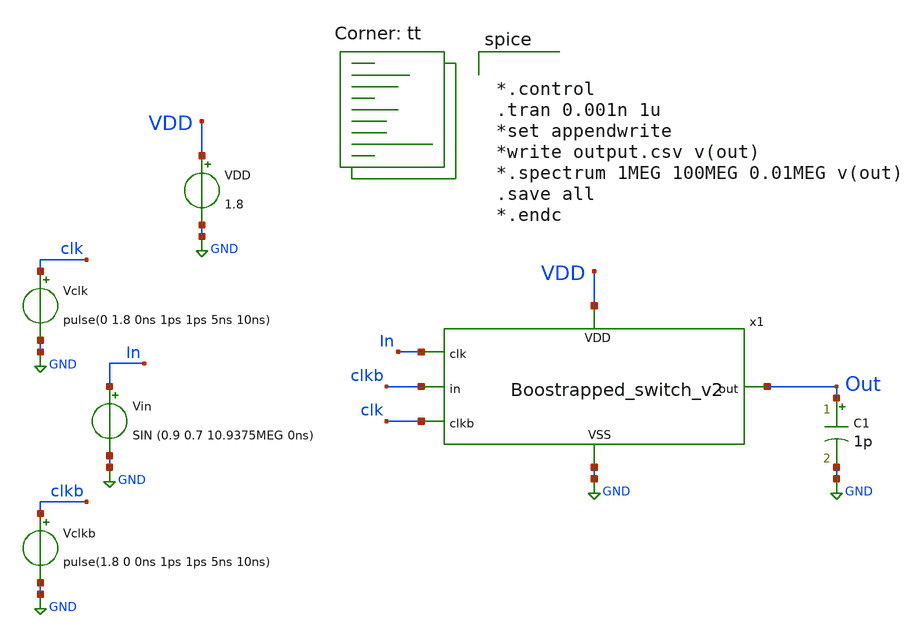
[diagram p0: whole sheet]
** sch_path: SampleHold/Boostrapped_switch_v2_tb.sch
**.subckt Boostrapped_switch_v2_tb
Vclk clk GND pulse(0 1.8 0ns 1ps 1ps 5ns 10ns)
Vin In GND SIN (0.9 0.7 10.9375MEG 0ns)
VDD VDD GND 1.8
Vclkb clkb GND pulse(1.8 0 0ns 1ps 1ps 5ns 10ns)
C1 Out GND 1p m=1
x1 clkb In clk GND Out VDD Boostrapped_switch_v2
**** begin user architecture code
.lib $::SKYWATER_MODELS/sky130.lib.spice tt


*.control
.tran 0.001n 1u
*set appendwrite
*write output.csv v(out)
*.spectrum 1MEG 100MEG 0.01MEG v(out)
.save all
*.endc


**** end user architecture code
**.ends

* expanding   symbol:  project/SampleHold/Boostrapped_switch_v2.sym # of pins=6
** sym_path: SampleHold/Boostrapped_switch_v2.sym
** sch_path: SampleHold/Boostrapped_switch_v2.sch
.subckt Boostrapped_switch_v2 in clk clkb VSS out VDD
*.ipin in
*.opin out
*.ipin VSS
*.ipin VDD
*.ipin clkb
*.ipin clk
XM1 net4 clkb net5 VSS sky130_fd_pr__nfet_01v8 L=0.15 W=2 nf=1 ad='int((nf+1)/2) * W/nf * 0.29' as='int((nf+2)/2) * W/nf * 0.29'
+ pd='2*int((nf+1)/2) * (W/nf + 0.29)' ps='2*int((nf+2)/2) * (W/nf + 0.29)' nrd='0.29 / W' nrs='0.29 / W'
+ sa=0 sb=0 sd=0 mult=1 m=1
XM2 in clk net4 VSS sky130_fd_pr__nfet_01v8 L=0.15 W=6 nf=1 ad='int((nf+1)/2) * W/nf * 0.29' as='int((nf+2)/2) * W/nf * 0.29'
+ pd='2*int((nf+1)/2) * (W/nf + 0.29)' ps='2*int((nf+2)/2) * (W/nf + 0.29)' nrd='0.29 / W' nrs='0.29 / W'
+ sa=0 sb=0 sd=0 mult=1 m=1
XM3 net1 Vg net2 net2 sky130_fd_pr__pfet_01v8 L=0.15 W=2 nf=1 ad='int((nf+1)/2) * W/nf * 0.29' as='int((nf+2)/2) * W/nf * 0.29'
+ pd='2*int((nf+1)/2) * (W/nf + 0.29)' ps='2*int((nf+2)/2) * (W/nf + 0.29)' nrd='0.29 / W' nrs='0.29 / W'
+ sa=0 sb=0 sd=0 mult=1 m=1
XM4 Vg clkb net2 net2 sky130_fd_pr__pfet_01v8 L=0.15 W=6 nf=1 ad='int((nf+1)/2) * W/nf * 0.29' as='int((nf+2)/2) * W/nf * 0.29'
+ pd='2*int((nf+1)/2) * (W/nf + 0.29)' ps='2*int((nf+2)/2) * (W/nf + 0.29)' nrd='0.29 / W' nrs='0.29 / W'
+ sa=0 sb=0 sd=0 mult=1 m=1
XM5 out Vg in VSS sky130_fd_pr__nfet_01v8 L=0.15 W=12 nf=1 ad='int((nf+1)/2) * W/nf * 0.29' as='int((nf+2)/2) * W/nf * 0.29'
+ pd='2*int((nf+1)/2) * (W/nf + 0.29)' ps='2*int((nf+2)/2) * (W/nf + 0.29)' nrd='0.29 / W' nrs='0.29 / W'
+ sa=0 sb=0 sd=0 mult=1 m=1
XM6 out clkb in VDD sky130_fd_pr__pfet_01v8 L=0.15 W=10 nf=1 ad='int((nf+1)/2) * W/nf * 0.29' as='int((nf+2)/2) * W/nf * 0.29'
+ pd='2*int((nf+1)/2) * (W/nf + 0.29)' ps='2*int((nf+2)/2) * (W/nf + 0.29)' nrd='0.29 / W' nrs='0.29 / W'
+ sa=0 sb=0 sd=0 mult=1 m=1
XM7 Vg VDD net3 VSS sky130_fd_pr__nfet_01v8 L=0.15 W=0.5 nf=1 ad='int((nf+1)/2) * W/nf * 0.29' as='int((nf+2)/2) * W/nf * 0.29'
+ pd='2*int((nf+1)/2) * (W/nf + 0.29)' ps='2*int((nf+2)/2) * (W/nf + 0.29)' nrd='0.29 / W' nrs='0.29 / W'
+ sa=0 sb=0 sd=0 mult=1 m=1
XM8 net3 clkb VSS VSS sky130_fd_pr__nfet_01v8 L=0.15 W=0.5 nf=1 ad='int((nf+1)/2) * W/nf * 0.29' as='int((nf+2)/2) * W/nf * 0.29'
+ pd='2*int((nf+1)/2) * (W/nf + 0.29)' ps='2*int((nf+2)/2) * (W/nf + 0.29)' nrd='0.29 / W' nrs='0.29 / W'
+ sa=0 sb=0 sd=0 mult=1 m=1
XC1 net4 net2 sky130_fd_pr__cap_mim_m3_1 W=20 L=6 MF=4 m=4
XM9 VDD clk net1 net1 sky130_fd_pr__pfet_01v8 L=0.15 W=2 nf=1 ad='int((nf+1)/2) * W/nf * 0.29' as='int((nf+2)/2) * W/nf * 0.29'
+ pd='2*int((nf+1)/2) * (W/nf + 0.29)' ps='2*int((nf+2)/2) * (W/nf + 0.29)' nrd='0.29 / W' nrs='0.29 / W'
+ sa=0 sb=0 sd=0 mult=1 m=1
XM10 net5 clkb VSS VSS sky130_fd_pr__nfet_01v8 L=0.15 W=2 nf=1 ad='int((nf+1)/2) * W/nf * 0.29' as='int((nf+2)/2) * W/nf * 0.29'
+ pd='2*int((nf+1)/2) * (W/nf + 0.29)' ps='2*int((nf+2)/2) * (W/nf + 0.29)' nrd='0.29 / W' nrs='0.29 / W'
+ sa=0 sb=0 sd=0 mult=1 m=1
.ends

.GLOBAL GND
.end
